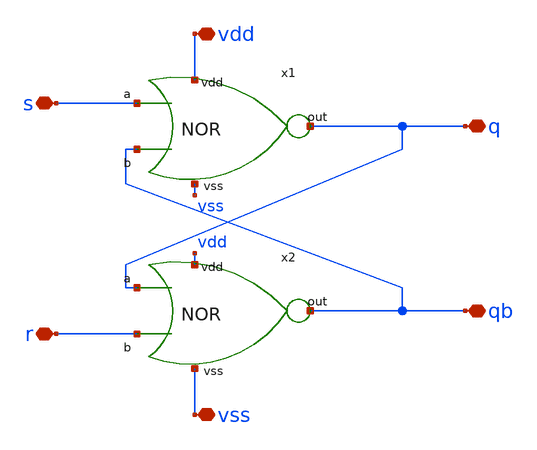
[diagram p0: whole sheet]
** sch_path: designs/libs/qw_core_analog/SRLATCH/SRLATCH.sch
**.subckt SRLATCH s r q qb vdd vss
*.iopin s
*.iopin r
*.iopin q
*.iopin qb
*.iopin vdd
*.iopin vss
x1 vdd s qb q vss NOR
x2 vdd q r qb vss NOR
**.ends

* expanding   symbol:  libs/qw_core_analog/NOR.sym # of pins=5
** sym_path: designs/libs/qw_core_analog_pkedit/NOR.sym
** sch_path: designs/libs/qw_core_analog_pkedit/NOR.sch
.subckt NOR vdd a b out vss
*.iopin vdd
*.iopin vss
*.iopin a
*.iopin b
*.iopin out
XM1 out a vss vss nfet_03v3 L=0.28u W=0.5u nf=1 ad='int((nf+1)/2) * W/nf * 0.18u' as='int((nf+2)/2) * W/nf * 0.18u'
+ pd='2*int((nf+1)/2) * (W/nf + 0.18u)' ps='2*int((nf+2)/2) * (W/nf + 0.18u)' nrd='0.18u / W' nrs='0.18u / W'
+ sa=0 sb=0 sd=0 m=1
XM2 net1 a vdd vdd pfet_03v3 L=0.28u W=2u nf=1 ad='int((nf+1)/2) * W/nf * 0.18u' as='int((nf+2)/2) * W/nf * 0.18u'
+ pd='2*int((nf+1)/2) * (W/nf + 0.18u)' ps='2*int((nf+2)/2) * (W/nf + 0.18u)' nrd='0.18u / W' nrs='0.18u / W'
+ sa=0 sb=0 sd=0 m=1
XM3 out b net1 vdd pfet_03v3 L=0.28u W=2u nf=1 ad='int((nf+1)/2) * W/nf * 0.18u' as='int((nf+2)/2) * W/nf * 0.18u'
+ pd='2*int((nf+1)/2) * (W/nf + 0.18u)' ps='2*int((nf+2)/2) * (W/nf + 0.18u)' nrd='0.18u / W' nrs='0.18u / W'
+ sa=0 sb=0 sd=0 m=1
XM4 out b vss vss nfet_03v3 L=0.28u W=0.5u nf=1 ad='int((nf+1)/2) * W/nf * 0.18u' as='int((nf+2)/2) * W/nf * 0.18u'
+ pd='2*int((nf+1)/2) * (W/nf + 0.18u)' ps='2*int((nf+2)/2) * (W/nf + 0.18u)' nrd='0.18u / W' nrs='0.18u / W'
+ sa=0 sb=0 sd=0 m=1
.ends

.end
